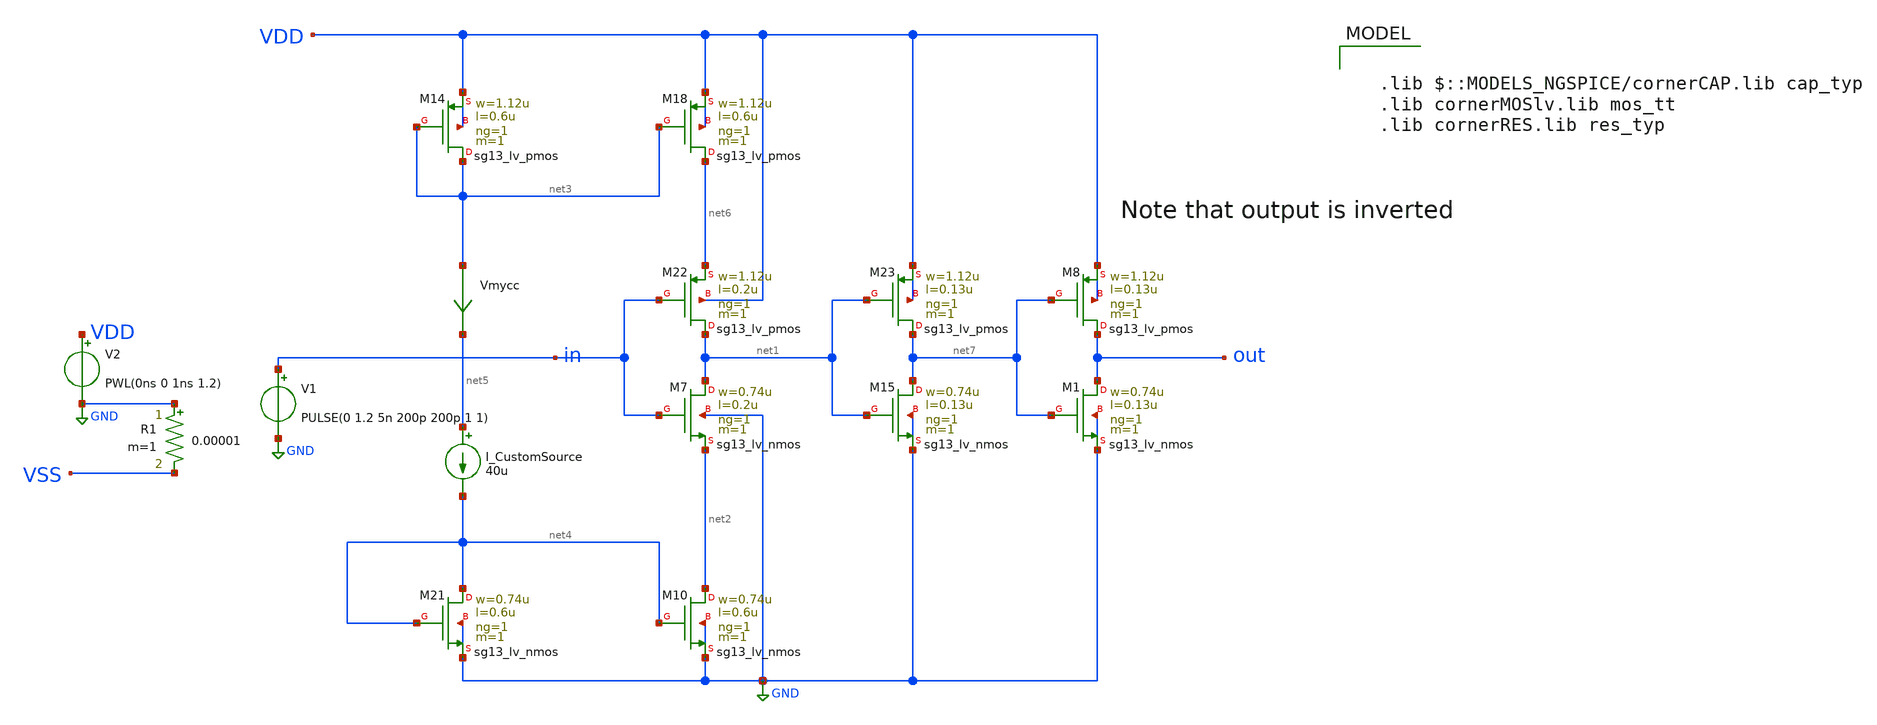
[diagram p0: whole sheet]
** sch_path: schematics/wip/delay_line_vary_current.sch
**.subckt delay_line_vary_current
XM7 net1 in net2 GND sg13_lv_nmos w=0.74u l=0.2u ng=1 m=1 mm_ok=1
XM10 net2 net4 GND GND sg13_lv_nmos w=0.74u l=0.6u ng=1 m=1 mm_ok=1
Vmycc net3 net5 0
.save i(vmycc)
XM18 net6 net3 VDD VDD sg13_lv_pmos w=1.12u l=0.6u ng=1 m=1 mm_ok=1
XM14 net3 net3 VDD VDD sg13_lv_pmos w=1.12u l=0.6u ng=1 m=1 mm_ok=1
XM15 net7 net1 GND GND sg13_lv_nmos w=0.74u l=0.13u ng=1 m=1 mm_ok=1
XM21 net4 net4 GND GND sg13_lv_nmos w=0.74u l=0.6u ng=1 m=1 mm_ok=1
XM22 net1 in net6 VDD sg13_lv_pmos w=1.12u l=0.2u ng=1 m=1 mm_ok=1
XM23 net7 net1 VDD VDD sg13_lv_pmos w=1.12u l=0.13u ng=1 m=1 mm_ok=1
I_CustomSource net5 net4 40u
V2 VDD GND PWL(0ns 0 1ns 1.2)
V1 in GND PULSE(0 1.2 5n 200p 200p 1 1)
R1 GND VSS 0.00001 m=1
XM1 out net7 GND GND sg13_lv_nmos w=0.74u l=0.13u ng=1 m=1 mm_ok=1
XM8 out net7 VDD VDD sg13_lv_pmos w=1.12u l=0.13u ng=1 m=1 mm_ok=1
**** begin user architecture code

  .lib $::MODELS_NGSPICE/cornerCAP.lib cap_typ
  .lib cornerMOSlv.lib mos_tt
  .lib cornerRES.lib res_typ



.options temp=27
.include sg13g2_stdcell.spice
.control
  * 1. Define the sweep parameters
  let i_start = 1e-6
  let i_stop = 30e-6
  let i_step = 1e-6
  let i_steps = (i_stop - i_start) / i_step + 1

  * 2. Create empty vectors to store our summary data
  let i_axis = unitvec(i_steps)
  let delay_results = unitvec(i_steps)
  let index = 0

  let i_act = i_start
  while i_act <= i_stop
    save all
    alter I_CustomSource i_act
    tran 5p 10n

    * Perform measurement
    * Please note that the output is inverted, so we detect FALLing edge
    meas tran tdiff TRIG v(in) VAL=0.6 RISE=1 TARG v(out) VAL=0.6 FALL=1

    let delay_results[index] = tdiff
    let i_axis[index] = i_act

    let i_act = i_act + i_step
    let index = index + 1


    write delay_line_vary_current.raw
  end

  * 4. Plot the results:
  plot delay_results vs i_axis title 'Ring Oscillator: Delay vs Bias current' xlabel 'I (A)' ylabel 'Delay (s)'
.endc


**** end user architecture code
**.ends
.GLOBAL GND
.end
